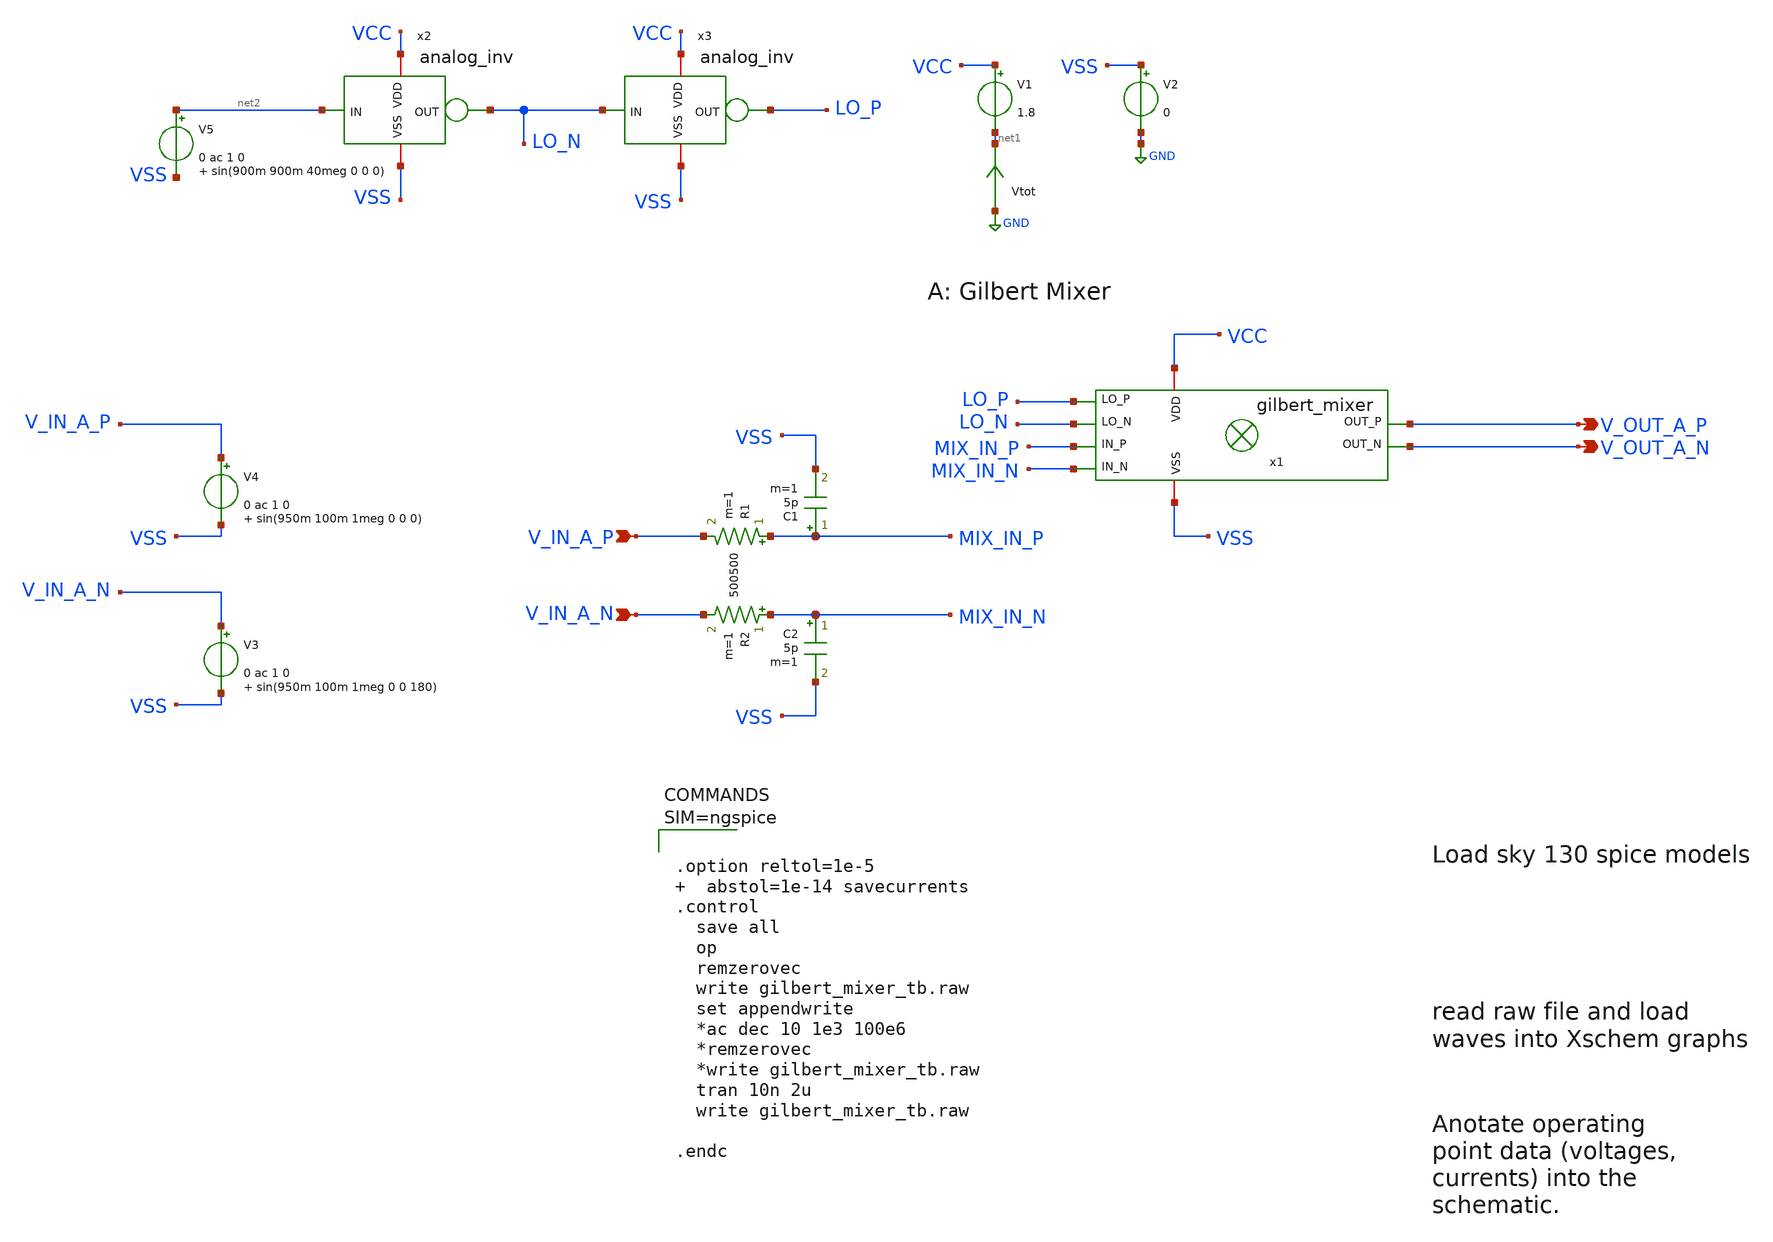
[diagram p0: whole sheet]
** sch_path: xschem/gilbert_mixer_tb.sch
**.subckt gilbert_mixer_tb V_IN_A_P V_OUT_A_N V_OUT_A_P V_IN_A_N
*.ipin V_IN_A_P
*.opin V_OUT_A_N
*.opin V_OUT_A_P
*.ipin V_IN_A_N
V1 VCC net1 1.8
V2 VSS GND 0
V4 V_IN_A_P VSS 0 ac 1 0 sin(950m 100m 1meg 0 0 0)
R1 MIX_IN_P V_IN_A_P 500 m=1
C1 MIX_IN_P VSS 5p m=1
R2 MIX_IN_N V_IN_A_N 500 m=1
C2 MIX_IN_N VSS 5p m=1
x1 VSS VCC V_OUT_A_N V_OUT_A_P LO_N LO_P MIX_IN_N MIX_IN_P gilbert_mixer
V5 net2 VSS 0 ac 1 0 sin(900m 900m 40meg 0 0 0)
x2 VCC net2 LO_N VSS analog_inv
x3 VCC LO_N LO_P VSS analog_inv
V3 V_IN_A_N VSS 0 ac 1 0 sin(950m 100m 1meg 0 0 180)
Vtot GND net1 0
.save i(vtot)
**** begin user architecture code

** opencircuitdesign pdks install
.lib $::SKYWATER_MODELS/sky130.lib.spice tt





.option reltol=1e-5   abstol=1e-14 savecurrents
.control
  save all
  op
  remzerovec
  write gilbert_mixer_tb.raw
  set appendwrite
  *ac dec 10 1e3 100e6
  *remzerovec
  *write gilbert_mixer_tb.raw
  tran 10n 2u
  write gilbert_mixer_tb.raw

.endc



**** end user architecture code
**.ends

* expanding   symbol:  gilbert_mixer.sym # of pins=8
** sym_path: xschem/gilbert_mixer.sym
** sch_path: xschem/gilbert_mixer.sch
.subckt gilbert_mixer VSS VDD OUT_N OUT_P LO_N LO_P IN_N IN_P
*.iopin VDD
*.iopin VSS
*.ipin LO_P
*.ipin LO_N
*.ipin IN_P
*.ipin IN_N
*.opin OUT_N
*.opin OUT_P
XR3 VSS NET_R3 net2 sky130_fd_pr__res_high_po_0p35 L=0.1 mult=30 m=30
XM2 OUT_P IN_N NET_M6_DRAIN VSS sky130_fd_pr__nfet_01v8 L=0.38 W=3.6 nf=2 ad='int((nf+1)/2) * W/nf * 0.29'
+ as='int((nf+2)/2) * W/nf * 0.29' pd='2*int((nf+1)/2) * (W/nf + 0.29)' ps='2*int((nf+2)/2) * (W/nf + 0.29)'
+ nrd='0.29 / W' nrs='0.29 / W' sa=0 sb=0 sd=0 mult=1 m=1
XM4 OUT_N IN_N NET_M5_DRAIN VSS sky130_fd_pr__nfet_01v8 L=0.38 W=3.6 nf=2 ad='int((nf+1)/2) * W/nf * 0.29'
+ as='int((nf+2)/2) * W/nf * 0.29' pd='2*int((nf+1)/2) * (W/nf + 0.29)' ps='2*int((nf+2)/2) * (W/nf + 0.29)'
+ nrd='0.29 / W' nrs='0.29 / W' sa=0 sb=0 sd=0 mult=1 m=1
XM6 NET_M6_DRAIN LO_N NET_R3 VSS sky130_fd_pr__nfet_01v8 L=0.38 W=3.6 nf=2 ad='int((nf+1)/2) * W/nf * 0.29'
+ as='int((nf+2)/2) * W/nf * 0.29' pd='2*int((nf+1)/2) * (W/nf + 0.29)' ps='2*int((nf+2)/2) * (W/nf + 0.29)'
+ nrd='0.29 / W' nrs='0.29 / W' sa=0 sb=0 sd=0 mult=1 m=1
XM1 OUT_N IN_P NET_M6_DRAIN VSS sky130_fd_pr__nfet_01v8 L=0.38 W=3.6 nf=2 ad='int((nf+1)/2) * W/nf * 0.29'
+ as='int((nf+2)/2) * W/nf * 0.29' pd='2*int((nf+1)/2) * (W/nf + 0.29)' ps='2*int((nf+2)/2) * (W/nf + 0.29)'
+ nrd='0.29 / W' nrs='0.29 / W' sa=0 sb=0 sd=0 mult=1 m=1
XM3 OUT_P IN_P NET_M5_DRAIN VSS sky130_fd_pr__nfet_01v8 L=0.38 W=3.6 nf=2 ad='int((nf+1)/2) * W/nf * 0.29'
+ as='int((nf+2)/2) * W/nf * 0.29' pd='2*int((nf+1)/2) * (W/nf + 0.29)' ps='2*int((nf+2)/2) * (W/nf + 0.29)'
+ nrd='0.29 / W' nrs='0.29 / W' sa=0 sb=0 sd=0 mult=1 m=1
XM5 NET_M5_DRAIN LO_P NET_R3 VSS sky130_fd_pr__nfet_01v8 L=0.38 W=3.6 nf=2 ad='int((nf+1)/2) * W/nf * 0.29'
+ as='int((nf+2)/2) * W/nf * 0.29' pd='2*int((nf+1)/2) * (W/nf + 0.29)' ps='2*int((nf+2)/2) * (W/nf + 0.29)'
+ nrd='0.29 / W' nrs='0.29 / W' sa=0 sb=0 sd=0 mult=1 m=1
XR1 OUT_N VDD VSS sky130_fd_pr__res_high_po_0p35 L=15.3 mult=2 m=2
XR2 OUT_P VDD net1 sky130_fd_pr__res_high_po_0p35 L=15.3 mult=2 m=2
.ends


* expanding   symbol:  analog_inv.sym # of pins=4
** sym_path: xschem/analog_inv.sym
** sch_path: xschem/analog_inv.sch
.subckt analog_inv VDD IN OUT VSS
*.iopin VDD
*.iopin VSS
*.ipin IN
*.opin OUT
XM2 OUT IN VSS VSS sky130_fd_pr__nfet_01v8 L=0.38 W=3.6 nf=2 ad='int((nf+1)/2) * W/nf * 0.29' as='int((nf+2)/2) * W/nf * 0.29'
+ pd='2*int((nf+1)/2) * (W/nf + 0.29)' ps='2*int((nf+2)/2) * (W/nf + 0.29)' nrd='0.29 / W' nrs='0.29 / W'
+ sa=0 sb=0 sd=0 mult=1 m=1
XM1 OUT IN VDD VDD sky130_fd_pr__pfet_01v8 L=0.38 W=3.6 nf=2 ad='int((nf+1)/2) * W/nf * 0.29' as='int((nf+2)/2) * W/nf * 0.29'
+ pd='2*int((nf+1)/2) * (W/nf + 0.29)' ps='2*int((nf+2)/2) * (W/nf + 0.29)' nrd='0.29 / W' nrs='0.29 / W'
+ sa=0 sb=0 sd=0 mult=1 m=1
.ends

.GLOBAL GND
.end
